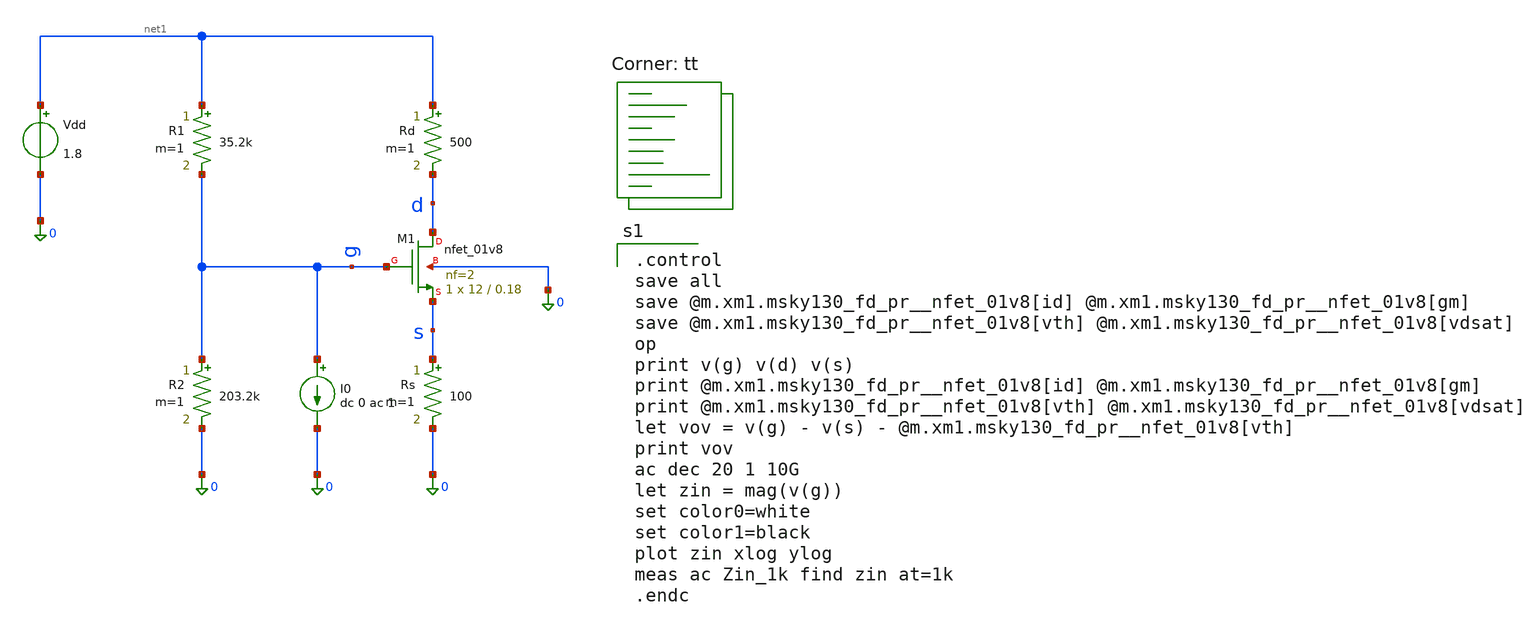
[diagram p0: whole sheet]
** sch_path: Homework 4 - Differential Pair Small Signal Gain/Simulations/ex2_final.sch
**.subckt ex2_final
XM1 d g s 0 sky130_fd_pr__nfet_01v8 L=0.18 W=12 nf=2 ad='int((2 + 1)/2) * 12 / 2 * 0.29' as='int((2 + 2)/2) * 12 / 2 * 0.29'
+ pd='2*int((2 + 1)/2) * (12 / 2 + 0.29)' ps='2*int((2 + 2)/2) * (12 / 2 + 0.29)' nrd='0.29 / 12 ' nrs='0.29 / 12 '
+ sa=0 sb=0 sd=0 mult=1 m=1
Rd net1 d 500 m=1
Rs s 0 100 m=1
Vdd net1 0 1.8
R1 net1 g 35.2k m=1
R2 g 0 203.2k m=1
I0 g 0 dc 0 ac 1
**** begin user architecture code
.lib $::SKYWATER_MODELS/sky130.lib.spice tt

.control
save all
save @m.xm1.msky130_fd_pr__nfet_01v8[id] @m.xm1.msky130_fd_pr__nfet_01v8[gm]
save @m.xm1.msky130_fd_pr__nfet_01v8[vth] @m.xm1.msky130_fd_pr__nfet_01v8[vdsat]
op
print v(g) v(d) v(s)
print @m.xm1.msky130_fd_pr__nfet_01v8[id] @m.xm1.msky130_fd_pr__nfet_01v8[gm]
print @m.xm1.msky130_fd_pr__nfet_01v8[vth] @m.xm1.msky130_fd_pr__nfet_01v8[vdsat]
let vov = v(g) - v(s) - @m.xm1.msky130_fd_pr__nfet_01v8[vth]
print vov
ac dec 20 1 10G
let zin = mag(v(g))
set color0=white
set color1=black
plot zin xlog ylog
meas ac Zin_1k find zin at=1k
.endc

**** end user architecture code
**.ends
.end
